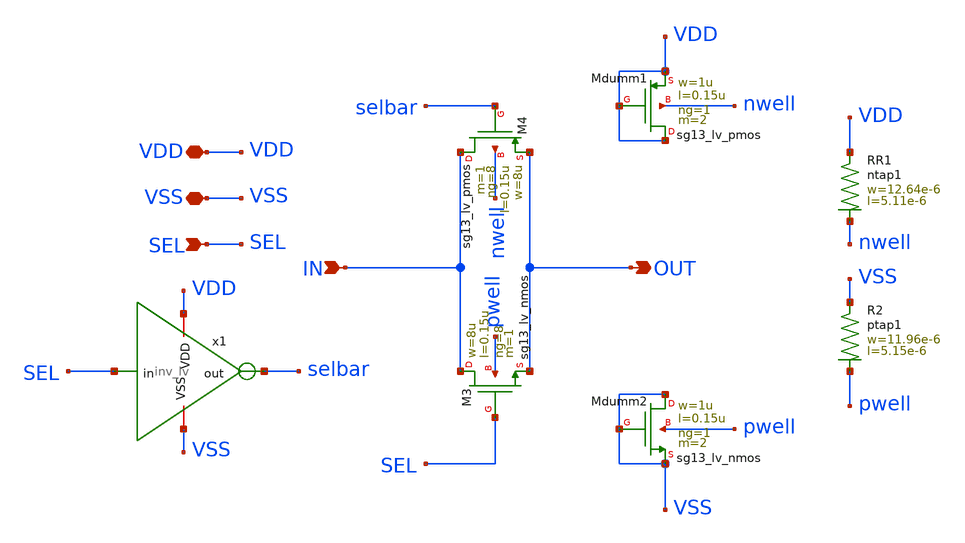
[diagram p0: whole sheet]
** sch_path: xschem/tg_lv_bak.sch
**.subckt tg_lv_bak IN VDD VSS OUT SEL
*.ipin IN
*.iopin VDD
*.iopin VSS
*.opin OUT
*.ipin SEL
x1 VDD SEL selbar VSS inv_lv
XM3 IN SEL OUT pwell sg13_lv_nmos w=8u l=0.15u ng=8 m=1 mm_ok=1
XM4 IN selbar OUT nwell sg13_lv_pmos w=8u l=0.15u ng=8 m=1 mm_ok=1
XMdumm1 VDD VDD VDD nwell sg13_lv_pmos w=1u l=0.15u ng=1 m=2 mm_ok=1
XMdumm2 VSS VSS VSS pwell sg13_lv_nmos w=1u l=0.15u ng=1 m=2 mm_ok=1
XR1 VDD nwell ntap1 R=9.791 w=12.64e-6 l=5.11e-6
XR2 VSS pwell ptap1 R=10.23 w=11.96e-6 l=5.15e-6
**.ends
.end
